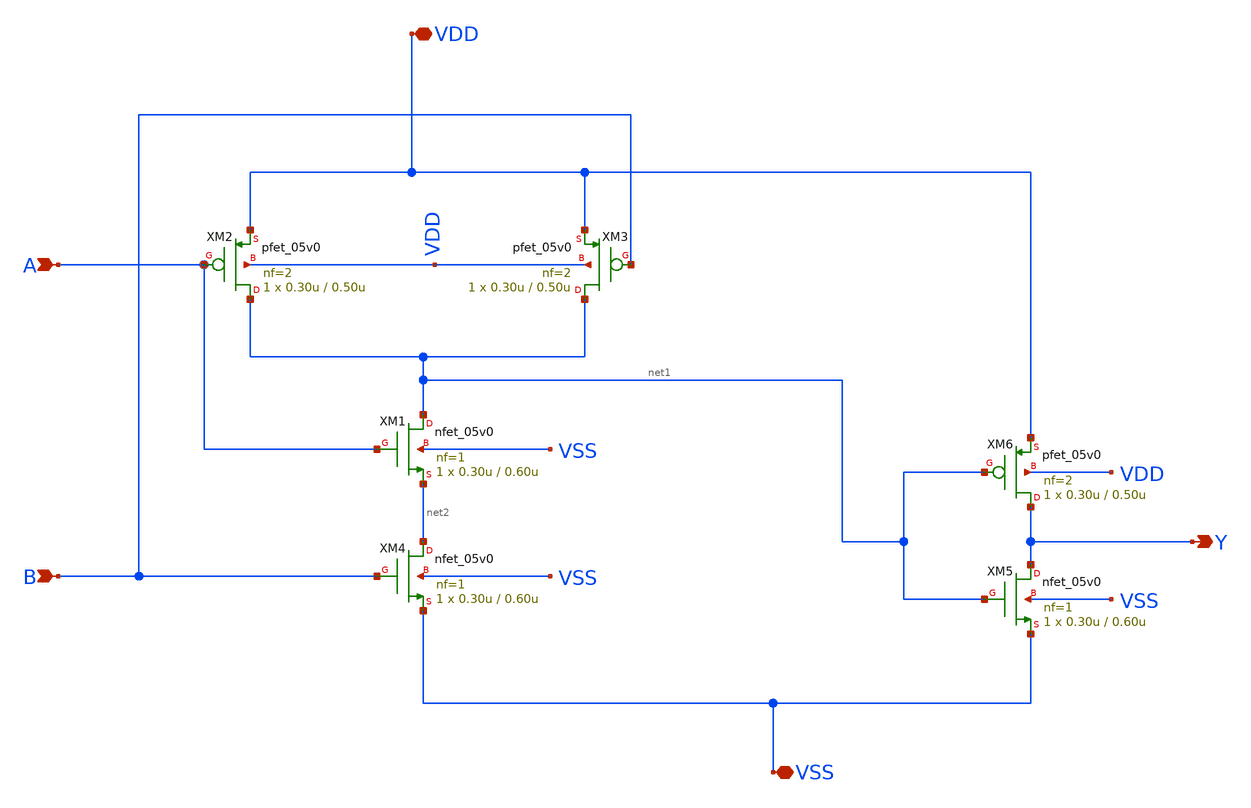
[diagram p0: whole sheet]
** sch_path: designs/libs/core_test/test_and/test_and.sch
**.subckt test_and A B VDD VSS Y
*.ipin A
*.ipin B
*.iopin VDD
*.iopin VSS
*.opin Y
XM1 net1 A net2 VSS nfet_05v0 L=0.60u W=0.30u nf=1 ad='int((nf+1)/2) * W/nf * 0.18u' as='int((nf+2)/2) * W/nf * 0.18u'
+ pd='2*int((nf+1)/2) * (W/nf + 0.18u)' ps='2*int((nf+2)/2) * (W/nf + 0.18u)' nrd='0.18u / W' nrs='0.18u / W'
+ sa=0 sb=0 sd=0 m=1
XM2 net1 A VDD VDD pfet_05v0 L=0.50u W=0.30u nf=2 ad='int((nf+1)/2) * W/nf * 0.18u' as='int((nf+2)/2) * W/nf * 0.18u'
+ pd='2*int((nf+1)/2) * (W/nf + 0.18u)' ps='2*int((nf+2)/2) * (W/nf + 0.18u)' nrd='0.18u / W' nrs='0.18u / W'
+ sa=0 sb=0 sd=0 m=1
XM3 net1 B VDD VDD pfet_05v0 L=0.50u W=0.30u nf=2 ad='int((nf+1)/2) * W/nf * 0.18u' as='int((nf+2)/2) * W/nf * 0.18u'
+ pd='2*int((nf+1)/2) * (W/nf + 0.18u)' ps='2*int((nf+2)/2) * (W/nf + 0.18u)' nrd='0.18u / W' nrs='0.18u / W'
+ sa=0 sb=0 sd=0 m=1
XM4 net2 B VSS VSS nfet_05v0 L=0.60u W=0.30u nf=1 ad='int((nf+1)/2) * W/nf * 0.18u' as='int((nf+2)/2) * W/nf * 0.18u'
+ pd='2*int((nf+1)/2) * (W/nf + 0.18u)' ps='2*int((nf+2)/2) * (W/nf + 0.18u)' nrd='0.18u / W' nrs='0.18u / W'
+ sa=0 sb=0 sd=0 m=1
XM5 Y net1 VSS VSS nfet_05v0 L=0.60u W=0.30u nf=1 ad='int((nf+1)/2) * W/nf * 0.18u' as='int((nf+2)/2) * W/nf * 0.18u'
+ pd='2*int((nf+1)/2) * (W/nf + 0.18u)' ps='2*int((nf+2)/2) * (W/nf + 0.18u)' nrd='0.18u / W' nrs='0.18u / W'
+ sa=0 sb=0 sd=0 m=1
XM6 Y net1 VDD VDD pfet_05v0 L=0.50u W=0.30u nf=2 ad='int((nf+1)/2) * W/nf * 0.18u' as='int((nf+2)/2) * W/nf * 0.18u'
+ pd='2*int((nf+1)/2) * (W/nf + 0.18u)' ps='2*int((nf+2)/2) * (W/nf + 0.18u)' nrd='0.18u / W' nrs='0.18u / W'
+ sa=0 sb=0 sd=0 m=1
**.ends
.end
